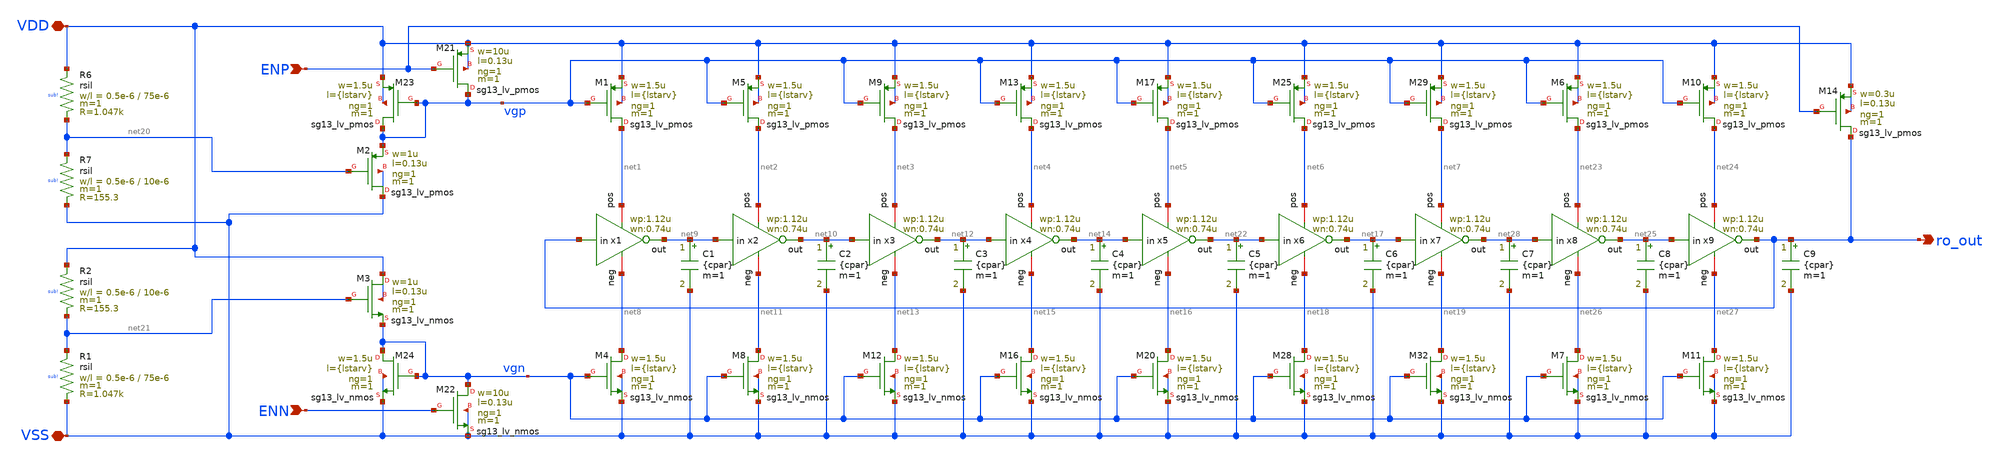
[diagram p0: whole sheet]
** sch_path: analog/temp-sens-core/temp_sens_core.sch
**.subckt temp_sens_core ro_out VDD VSS ENP ENN
*.opin ro_out
*.iopin VDD
*.iopin VSS
*.ipin ENP
*.ipin ENN
XM1 net1 vgp VDD VDD sg13_lv_pmos w=1.5u l={lstarv} ng=1 m=1 mm_ok=1
XM21 vgp ENP VDD VDD sg13_lv_pmos w=10u l=0.13u ng=1 m=1 mm_ok=1
XM22 vgn ENN VSS VSS sg13_lv_nmos w=10u l=0.13u ng=1 m=1 mm_ok=1
XM23 vgp vgp VDD VDD sg13_lv_pmos w=1.5u l={lstarv} ng=1 m=1 mm_ok=1
XM24 vgn vgn VSS VSS sg13_lv_nmos w=1.5u l={lstarv} ng=1 m=1 mm_ok=1
XM4 net8 vgn VSS VSS sg13_lv_nmos w=1.5u l={lstarv} ng=1 m=1 mm_ok=1
XM5 net2 vgp VDD VDD sg13_lv_pmos w=1.5u l={lstarv} ng=1 m=1 mm_ok=1
XM8 net11 vgn VSS VSS sg13_lv_nmos w=1.5u l={lstarv} ng=1 m=1 mm_ok=1
XM9 net3 vgp VDD VDD sg13_lv_pmos w=1.5u l={lstarv} ng=1 m=1 mm_ok=1
XM12 net13 vgn VSS VSS sg13_lv_nmos w=1.5u l={lstarv} ng=1 m=1 mm_ok=1
XM13 net4 vgp VDD VDD sg13_lv_pmos w=1.5u l={lstarv} ng=1 m=1 mm_ok=1
XM16 net15 vgn VSS VSS sg13_lv_nmos w=1.5u l={lstarv} ng=1 m=1 mm_ok=1
XM17 net5 vgp VDD VDD sg13_lv_pmos w=1.5u l={lstarv} ng=1 m=1 mm_ok=1
XM20 net16 vgn VSS VSS sg13_lv_nmos w=1.5u l={lstarv} ng=1 m=1 mm_ok=1
XM25 net6 vgp VDD VDD sg13_lv_pmos w=1.5u l={lstarv} ng=1 m=1 mm_ok=1
XM28 net18 vgn VSS VSS sg13_lv_nmos w=1.5u l={lstarv} ng=1 m=1 mm_ok=1
XM29 net7 vgp VDD VDD sg13_lv_pmos w=1.5u l={lstarv} ng=1 m=1 mm_ok=1
XM32 net19 vgn VSS VSS sg13_lv_nmos w=1.5u l={lstarv} ng=1 m=1 mm_ok=1
x1 net1 ro_out net9 net8 inverter wp=1.12u wn=0.74u
x2 net2 net9 net10 net11 inverter wp=1.12u wn=0.74u
x3 net3 net10 net12 net13 inverter wp=1.12u wn=0.74u
x4 net4 net12 net14 net15 inverter wp=1.12u wn=0.74u
x5 net5 net14 net22 net16 inverter wp=1.12u wn=0.74u
x6 net6 net22 net17 net18 inverter wp=1.12u wn=0.74u
x7 net7 net17 net28 net19 inverter wp=1.12u wn=0.74u
XM2 VSS net20 vgp VSS sg13_lv_pmos w=1u l=0.13u ng=1 m=1 mm_ok=1
XM3 VDD net21 vgn VDD sg13_lv_nmos w=1u l=0.13u ng=1 m=1 mm_ok=1
XR6 VDD net20 sub! rsil w=0.5e-6 l=75e-6 m=1 mm_ok=1
XR7 net20 VSS sub! rsil w=0.5e-6 l=10e-6 m=1 mm_ok=1
XR1 net21 VSS sub! rsil w=0.5e-6 l=75e-6 m=1 mm_ok=1
XR2 VDD net21 sub! rsil w=0.5e-6 l=10e-6 m=1 mm_ok=1
C1 net9 VSS {cpar} m=1
C2 net10 VSS {cpar} m=1
C3 net12 VSS {cpar} m=1
C4 net14 VSS {cpar} m=1
C5 net22 VSS {cpar} m=1
C6 net17 VSS {cpar} m=1
C7 net28 VSS {cpar} m=1
XM6 net23 vgp VDD VDD sg13_lv_pmos w=1.5u l={lstarv} ng=1 m=1 mm_ok=1
XM7 net26 vgn VSS VSS sg13_lv_nmos w=1.5u l={lstarv} ng=1 m=1 mm_ok=1
XM10 net24 vgp VDD VDD sg13_lv_pmos w=1.5u l={lstarv} ng=1 m=1 mm_ok=1
XM11 net27 vgn VSS VSS sg13_lv_nmos w=1.5u l={lstarv} ng=1 m=1 mm_ok=1
x8 net23 net28 net25 net26 inverter wp=1.12u wn=0.74u
x9 net24 net25 ro_out net27 inverter wp=1.12u wn=0.74u
C8 net25 VSS {cpar} m=1
C9 ro_out VSS {cpar} m=1
XM14 ro_out ENP VDD VDD sg13_lv_pmos w=0.3u l=0.13u ng=1 m=1 mm_ok=1
**.ends

* expanding   symbol:  analog/inverter/inverter.sym # of pins=4
** sym_path: TSENSE8490-main/schematic/xschem/analog/inverter/inverter.sym
** sch_path: TSENSE8490-main/schematic/xschem/analog/inverter/inverter.sch
.subckt inverter pos in out neg  wp=0.74u wn=1.12u
*.ipin in
*.iopin pos
*.iopin neg
*.opin out
XM1 out in neg neg sg13_lv_nmos w={wn} l=0.13u ng=1 m=1 mm_ok=1
XM2 pos in out pos sg13_lv_pmos w={wp} l=0.13u ng=1 m=1 mm_ok=1
.ends

.end
